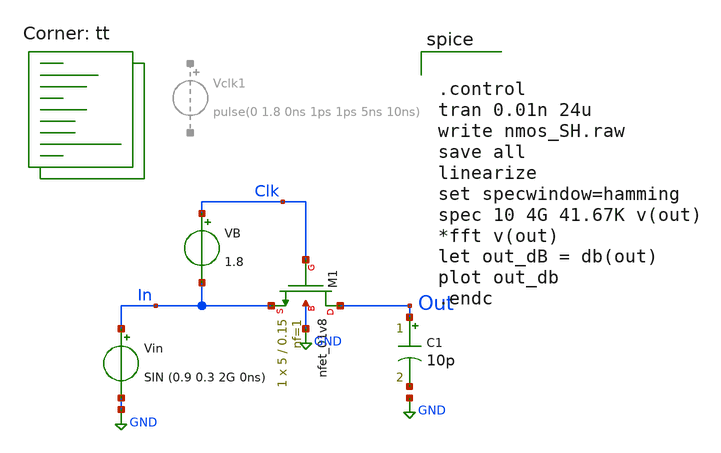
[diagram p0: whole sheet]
** sch_path: SampleHold/nmos_SH.sch
**.subckt nmos_SH
XM1 Out Clk In GND sky130_fd_pr__nfet_01v8 L=0.15 W=5 nf=1 ad='int((nf+1)/2) * W/nf * 0.29' as='int((nf+2)/2) * W/nf * 0.29'
+ pd='2*int((nf+1)/2) * (W/nf + 0.29)' ps='2*int((nf+2)/2) * (W/nf + 0.29)' nrd='0.29 / W' nrs='0.29 / W'
+ sa=0 sb=0 sd=0 mult=1 m=1
C1 Out net1 10p m=1
VB Clk In 1.8
Vin In GND SIN (0.9 0.3 2G 0ns)
**** begin user architecture code
.lib $::SKYWATER_MODELS/sky130.lib.spice tt


.control
tran 0.01n 24u
write nmos_SH.raw
save all
linearize
set specwindow=hamming
spec 10 4G 41.67K v(out)
*fft v(out)
let out_dB = db(out)
plot out_db
.endc


**** end user architecture code
**.ends
.GLOBAL GND
.end
